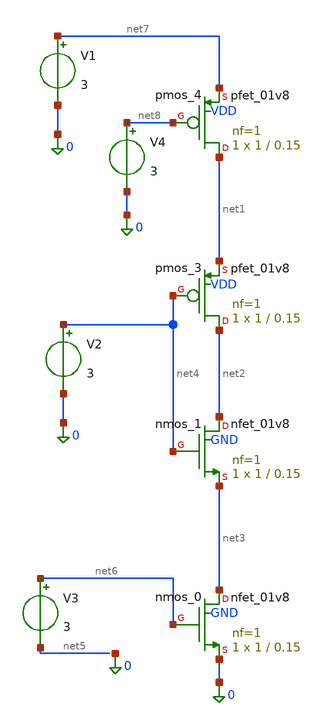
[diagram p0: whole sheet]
** sch_path: golden_netlists/10_1109_ACCESS_2019_2905767_06_001_crop1.sch
**.subckt 10_1109_ACCESS_2019_2905767_06_001_crop1
Xnmos_0 net3 net6 0 GND sky130_fd_pr__nfet_01v8 L=0.15 W=1 nf=1 ad='int((nf+1)/2) * W/nf * 0.29' as='int((nf+2)/2) * W/nf * 0.29'
+ pd='2*int((nf+1)/2) * (W/nf + 0.29)' ps='2*int((nf+2)/2) * (W/nf + 0.29)' nrd='0.29 / W' nrs='0.29 / W'
+ sa=0 sb=0 sd=0 mult=1 m=1
Xnmos_1 net2 net4 net3 GND sky130_fd_pr__nfet_01v8 L=0.15 W=1 nf=1 ad='int((nf+1)/2) * W/nf * 0.29' as='int((nf+2)/2) * W/nf * 0.29'
+ pd='2*int((nf+1)/2) * (W/nf + 0.29)' ps='2*int((nf+2)/2) * (W/nf + 0.29)' nrd='0.29 / W' nrs='0.29 / W'
+ sa=0 sb=0 sd=0 mult=1 m=1
Xpmos_3 net2 net4 net1 VDD sky130_fd_pr__pfet_01v8 L=0.15 W=1 nf=1 ad='int((1 + 1)/2) * 1 / 1 * 0.29'
+ as='int((1 + 2)/2) * 1 / 1 * 0.29' pd='2*int((1 + 1)/2) * (1 / 1 + 0.29)' ps='2*int((1 + 2)/2) * (1 / 1 + 0.29)'
+ nrd='0.29 / 1 ' nrs='0.29 / 1 ' sa=0 sb=0 sd=0 mult=1 m=1
Xpmos_4 net1 net8 net7 VDD sky130_fd_pr__pfet_01v8 L=0.15 W=1 nf=1 ad='int((1 + 1)/2) * 1 / 1 * 0.29'
+ as='int((1 + 2)/2) * 1 / 1 * 0.29' pd='2*int((1 + 1)/2) * (1 / 1 + 0.29)' ps='2*int((1 + 2)/2) * (1 / 1 + 0.29)'
+ nrd='0.29 / 1 ' nrs='0.29 / 1 ' sa=0 sb=0 sd=0 mult=1 m=1
V1 net7 0 3
V2 net4 0 3
V3 net6 net5 3
V4 net8 0 3
**.ends
.end
